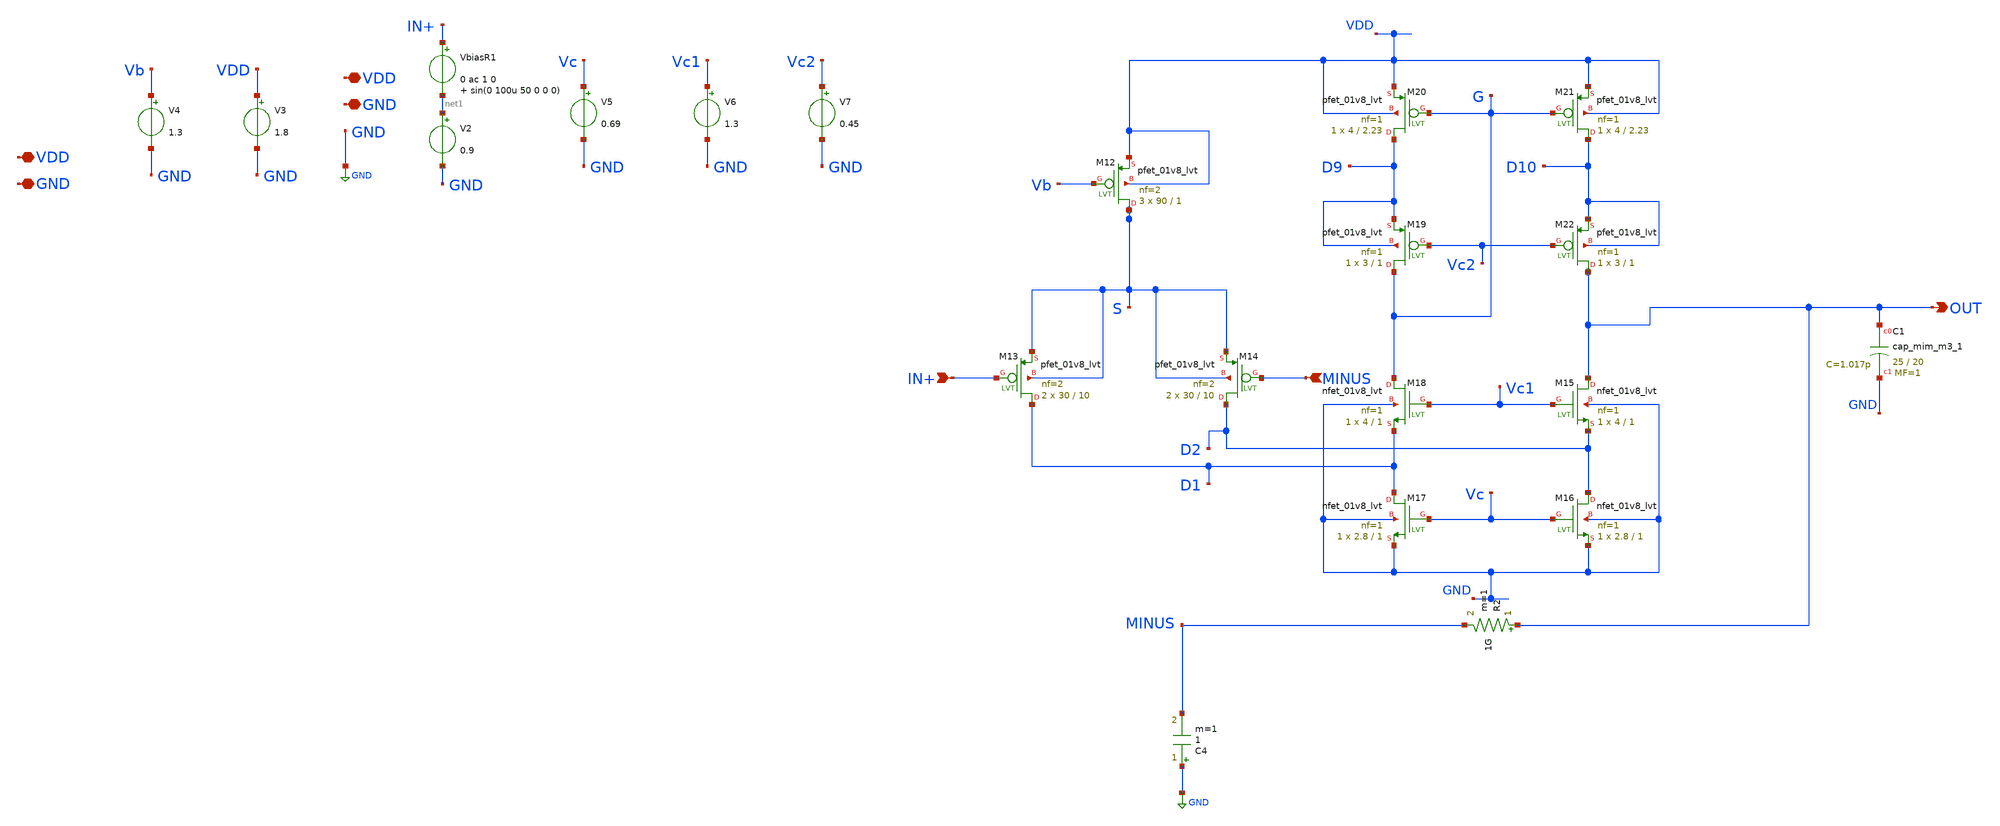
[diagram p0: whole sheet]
** sch_path: xschem/OTA_FoldedCascode_AC2.sch
**.subckt OTA_FoldedCascode_AC2 VDD GND VDD GND OUT IN+ MINUS
*.iopin VDD
*.iopin GND
*.iopin VDD
*.iopin GND
*.opin OUT
*.ipin IN+
*.ipin MINUS
VbiasR1 IN+ net1 0 ac 1 0 sin(0 100u 50 0 0 0)
V2 net1 GND 0.9
V3 VDD GND 1.8
V4 Vb GND 1.3
V5 Vc GND 0.69
V6 Vc1 GND 1.3
V7 Vc2 GND 0.45
XC1 OUT GND sky130_fd_pr__cap_mim_m3_1 W=25 L=20 MF=1 m=1
C4 GND MINUS 1 m=1
R2 OUT MINUS 1G m=1
XM12 S Vb VDD VDD sky130_fd_pr__pfet_01v8_lvt L=1 W=90 nf=2 ad='int((nf+1)/2) * W/nf * 0.29' as='int((nf+2)/2) * W/nf * 0.29'
+ pd='2*int((nf+1)/2) * (W/nf + 0.29)' ps='2*int((nf+2)/2) * (W/nf + 0.29)' nrd='0.29 / W' nrs='0.29 / W'
+ sa=0 sb=0 sd=0 mult=3 m=3
XM13 D1 IN+ S S sky130_fd_pr__pfet_01v8_lvt L=10 W=30 nf=2 ad='int((nf+1)/2) * W/nf * 0.29' as='int((nf+2)/2) * W/nf * 0.29'
+ pd='2*int((nf+1)/2) * (W/nf + 0.29)' ps='2*int((nf+2)/2) * (W/nf + 0.29)' nrd='0.29 / W' nrs='0.29 / W'
+ sa=0 sb=0 sd=0 mult=2 m=2
XM14 D2 MINUS S S sky130_fd_pr__pfet_01v8_lvt L=10 W=30 nf=2 ad='int((nf+1)/2) * W/nf * 0.29' as='int((nf+2)/2) * W/nf * 0.29'
+ pd='2*int((nf+1)/2) * (W/nf + 0.29)' ps='2*int((nf+2)/2) * (W/nf + 0.29)' nrd='0.29 / W' nrs='0.29 / W'
+ sa=0 sb=0 sd=0 mult=2 m=2
XM15 OUT Vc1 D2 GND sky130_fd_pr__nfet_01v8_lvt L=1 W=4 nf=1 ad='int((nf+1)/2) * W/nf * 0.29' as='int((nf+2)/2) * W/nf * 0.29'
+ pd='2*int((nf+1)/2) * (W/nf + 0.29)' ps='2*int((nf+2)/2) * (W/nf + 0.29)' nrd='0.29 / W' nrs='0.29 / W'
+ sa=0 sb=0 sd=0 mult=1 m=1
XM16 D2 Vc GND GND sky130_fd_pr__nfet_01v8_lvt L=1 W=2.8 nf=1 ad='int((nf+1)/2) * W/nf * 0.29' as='int((nf+2)/2) * W/nf * 0.29'
+ pd='2*int((nf+1)/2) * (W/nf + 0.29)' ps='2*int((nf+2)/2) * (W/nf + 0.29)' nrd='0.29 / W' nrs='0.29 / W'
+ sa=0 sb=0 sd=0 mult=1 m=1
XM17 D1 Vc GND GND sky130_fd_pr__nfet_01v8_lvt L=1 W=2.8 nf=1 ad='int((nf+1)/2) * W/nf * 0.29' as='int((nf+2)/2) * W/nf * 0.29'
+ pd='2*int((nf+1)/2) * (W/nf + 0.29)' ps='2*int((nf+2)/2) * (W/nf + 0.29)' nrd='0.29 / W' nrs='0.29 / W'
+ sa=0 sb=0 sd=0 mult=1 m=1
XM18 G Vc1 D1 GND sky130_fd_pr__nfet_01v8_lvt L=1 W=4 nf=1 ad='int((nf+1)/2) * W/nf * 0.29' as='int((nf+2)/2) * W/nf * 0.29'
+ pd='2*int((nf+1)/2) * (W/nf + 0.29)' ps='2*int((nf+2)/2) * (W/nf + 0.29)' nrd='0.29 / W' nrs='0.29 / W'
+ sa=0 sb=0 sd=0 mult=1 m=1
XM19 G Vc2 D9 D9 sky130_fd_pr__pfet_01v8_lvt L=1 W=3 nf=1 ad='int((nf+1)/2) * W/nf * 0.29' as='int((nf+2)/2) * W/nf * 0.29'
+ pd='2*int((nf+1)/2) * (W/nf + 0.29)' ps='2*int((nf+2)/2) * (W/nf + 0.29)' nrd='0.29 / W' nrs='0.29 / W'
+ sa=0 sb=0 sd=0 mult=1 m=1
XM20 D9 G VDD VDD sky130_fd_pr__pfet_01v8_lvt L=2.23 W=4 nf=1 ad='int((nf+1)/2) * W/nf * 0.29' as='int((nf+2)/2) * W/nf * 0.29'
+ pd='2*int((nf+1)/2) * (W/nf + 0.29)' ps='2*int((nf+2)/2) * (W/nf + 0.29)' nrd='0.29 / W' nrs='0.29 / W'
+ sa=0 sb=0 sd=0 mult=1 m=1
XM21 D10 G VDD VDD sky130_fd_pr__pfet_01v8_lvt L=2.23 W=4 nf=1 ad='int((nf+1)/2) * W/nf * 0.29' as='int((nf+2)/2) * W/nf * 0.29'
+ pd='2*int((nf+1)/2) * (W/nf + 0.29)' ps='2*int((nf+2)/2) * (W/nf + 0.29)' nrd='0.29 / W' nrs='0.29 / W'
+ sa=0 sb=0 sd=0 mult=1 m=1
XM22 OUT Vc2 D10 D10 sky130_fd_pr__pfet_01v8_lvt L=1 W=3 nf=1 ad='int((nf+1)/2) * W/nf * 0.29' as='int((nf+2)/2) * W/nf * 0.29'
+ pd='2*int((nf+1)/2) * (W/nf + 0.29)' ps='2*int((nf+2)/2) * (W/nf + 0.29)' nrd='0.29 / W' nrs='0.29 / W'
+ sa=0 sb=0 sd=0 mult=1 m=1
**** begin user architecture code



.option reltol=1e-5   abstol=1e-14 savecurrents
.control
  save all
  op
  remzerovec
  write OTA_FoldedCascode_AC2.raw

  set appendwrite
  ac dec 10 1 1e9
  remzerovec
  write OTA_FoldedCascode_AC2.raw

  tran 100u 100m
  write OTA_FoldedCascode_AC2.raw

.endc



.lib $::SKYWATER_MODELS/sky130.lib.spice tt
**** end user architecture code
**.ends
.GLOBAL GND
.end
